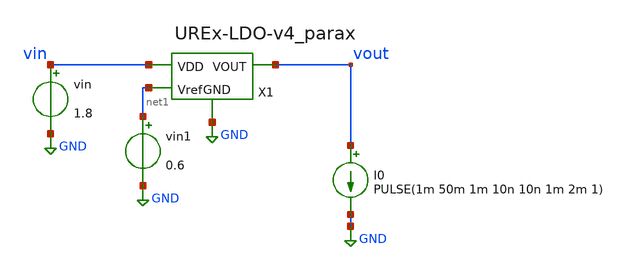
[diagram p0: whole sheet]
** sch_path: xschem/testbenches/postlayout/LoadReg-v4-postlayout.sch
**.subckt LoadReg-v4-postlayout
vin vin GND 1.8
X1 vin vout GND net1 UREx-LDO-v4_parax
I0 vout GND PULSE(1m 50m 1m 10n 10n 1m 2m 1)
vin1 net1 GND 0.6
**** begin user architecture code



.lib /usr/local/share/pdk/sky130A/libs.tech/ngspice/sky130.lib.spice tt
.param amp=0.01 freq=1k
.tran 1u 3m

.control
run
plot v(vout)
.endc


**** end user architecture code
**.ends

* expanding   symbol:  UREx-LDO-v4_parax.sym # of pins=4
** sym_path: xschem/UREx-LDO-v4.sym
.include [file normalize UREx-LDO-v4_parax.spice]
.GLOBAL GND
.end
